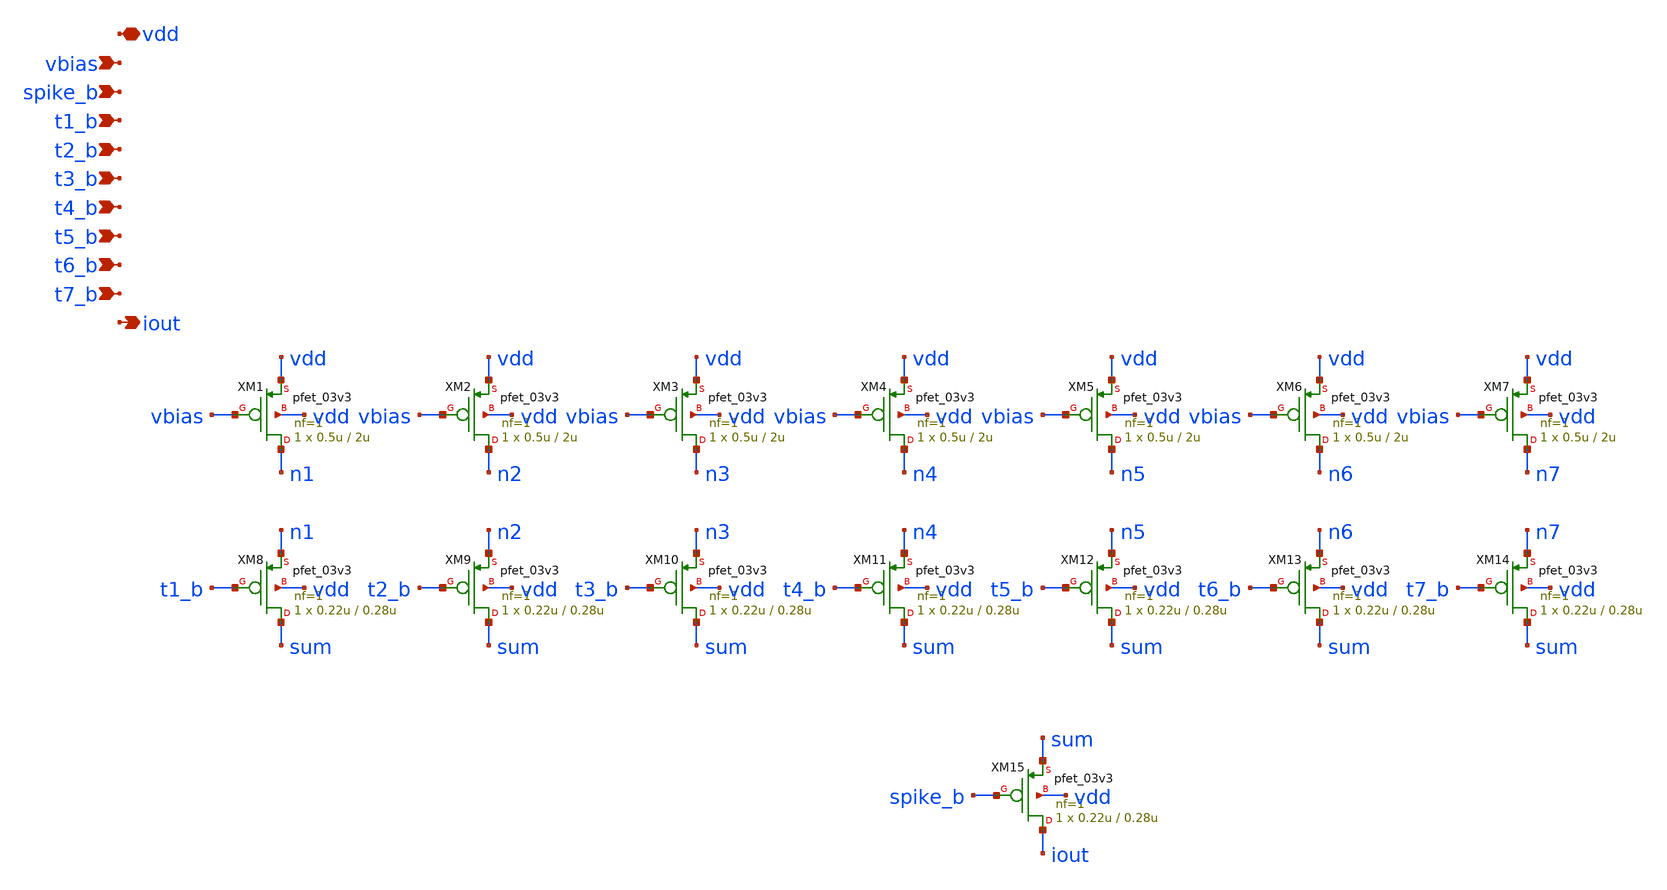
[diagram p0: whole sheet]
** sch_path: analog/dac/unary_DAC.sch
**.subckt unary_DAC vdd vbias spike_b t1_b t2_b t3_b t4_b t5_b t6_b t7_b iout
*.iopin vdd
*.ipin vbias
*.ipin spike_b
*.ipin t1_b
*.ipin t2_b
*.ipin t3_b
*.ipin t4_b
*.ipin t5_b
*.ipin t6_b
*.ipin t7_b
*.opin iout
XM1 n1 vbias vdd vdd pfet_03v3 L=2u W=0.5u nf=1 ad='int((nf+1)/2) * W/nf * 0.18u' as='int((nf+2)/2) * W/nf * 0.18u'
+ pd='2*int((nf+1)/2) * (W/nf + 0.18u)' ps='2*int((nf+2)/2) * (W/nf + 0.18u)' nrd='0.18u / W' nrs='0.18u / W'
+ sa=0 sb=0 sd=0 m=1
XM8 sum t1_b n1 vdd pfet_03v3 L=0.28u W=0.22u nf=1 ad='int((nf+1)/2) * W/nf * 0.18u' as='int((nf+2)/2) * W/nf * 0.18u'
+ pd='2*int((nf+1)/2) * (W/nf + 0.18u)' ps='2*int((nf+2)/2) * (W/nf + 0.18u)' nrd='0.18u / W' nrs='0.18u / W'
+ sa=0 sb=0 sd=0 m=1
XM2 n2 vbias vdd vdd pfet_03v3 L=2u W=0.5u nf=1 ad='int((nf+1)/2) * W/nf * 0.18u' as='int((nf+2)/2) * W/nf * 0.18u'
+ pd='2*int((nf+1)/2) * (W/nf + 0.18u)' ps='2*int((nf+2)/2) * (W/nf + 0.18u)' nrd='0.18u / W' nrs='0.18u / W'
+ sa=0 sb=0 sd=0 m=1
XM9 sum t2_b n2 vdd pfet_03v3 L=0.28u W=0.22u nf=1 ad='int((nf+1)/2) * W/nf * 0.18u' as='int((nf+2)/2) * W/nf * 0.18u'
+ pd='2*int((nf+1)/2) * (W/nf + 0.18u)' ps='2*int((nf+2)/2) * (W/nf + 0.18u)' nrd='0.18u / W' nrs='0.18u / W'
+ sa=0 sb=0 sd=0 m=1
XM3 n3 vbias vdd vdd pfet_03v3 L=2u W=0.5u nf=1 ad='int((nf+1)/2) * W/nf * 0.18u' as='int((nf+2)/2) * W/nf * 0.18u'
+ pd='2*int((nf+1)/2) * (W/nf + 0.18u)' ps='2*int((nf+2)/2) * (W/nf + 0.18u)' nrd='0.18u / W' nrs='0.18u / W'
+ sa=0 sb=0 sd=0 m=1
XM10 sum t3_b n3 vdd pfet_03v3 L=0.28u W=0.22u nf=1 ad='int((nf+1)/2) * W/nf * 0.18u' as='int((nf+2)/2) * W/nf * 0.18u'
+ pd='2*int((nf+1)/2) * (W/nf + 0.18u)' ps='2*int((nf+2)/2) * (W/nf + 0.18u)' nrd='0.18u / W' nrs='0.18u / W'
+ sa=0 sb=0 sd=0 m=1
XM4 n4 vbias vdd vdd pfet_03v3 L=2u W=0.5u nf=1 ad='int((nf+1)/2) * W/nf * 0.18u' as='int((nf+2)/2) * W/nf * 0.18u'
+ pd='2*int((nf+1)/2) * (W/nf + 0.18u)' ps='2*int((nf+2)/2) * (W/nf + 0.18u)' nrd='0.18u / W' nrs='0.18u / W'
+ sa=0 sb=0 sd=0 m=1
XM11 sum t4_b n4 vdd pfet_03v3 L=0.28u W=0.22u nf=1 ad='int((nf+1)/2) * W/nf * 0.18u' as='int((nf+2)/2) * W/nf * 0.18u'
+ pd='2*int((nf+1)/2) * (W/nf + 0.18u)' ps='2*int((nf+2)/2) * (W/nf + 0.18u)' nrd='0.18u / W' nrs='0.18u / W'
+ sa=0 sb=0 sd=0 m=1
XM5 n5 vbias vdd vdd pfet_03v3 L=2u W=0.5u nf=1 ad='int((nf+1)/2) * W/nf * 0.18u' as='int((nf+2)/2) * W/nf * 0.18u'
+ pd='2*int((nf+1)/2) * (W/nf + 0.18u)' ps='2*int((nf+2)/2) * (W/nf + 0.18u)' nrd='0.18u / W' nrs='0.18u / W'
+ sa=0 sb=0 sd=0 m=1
XM12 sum t5_b n5 vdd pfet_03v3 L=0.28u W=0.22u nf=1 ad='int((nf+1)/2) * W/nf * 0.18u' as='int((nf+2)/2) * W/nf * 0.18u'
+ pd='2*int((nf+1)/2) * (W/nf + 0.18u)' ps='2*int((nf+2)/2) * (W/nf + 0.18u)' nrd='0.18u / W' nrs='0.18u / W'
+ sa=0 sb=0 sd=0 m=1
XM6 n6 vbias vdd vdd pfet_03v3 L=2u W=0.5u nf=1 ad='int((nf+1)/2) * W/nf * 0.18u' as='int((nf+2)/2) * W/nf * 0.18u'
+ pd='2*int((nf+1)/2) * (W/nf + 0.18u)' ps='2*int((nf+2)/2) * (W/nf + 0.18u)' nrd='0.18u / W' nrs='0.18u / W'
+ sa=0 sb=0 sd=0 m=1
XM13 sum t6_b n6 vdd pfet_03v3 L=0.28u W=0.22u nf=1 ad='int((nf+1)/2) * W/nf * 0.18u' as='int((nf+2)/2) * W/nf * 0.18u'
+ pd='2*int((nf+1)/2) * (W/nf + 0.18u)' ps='2*int((nf+2)/2) * (W/nf + 0.18u)' nrd='0.18u / W' nrs='0.18u / W'
+ sa=0 sb=0 sd=0 m=1
XM7 n7 vbias vdd vdd pfet_03v3 L=2u W=0.5u nf=1 ad='int((nf+1)/2) * W/nf * 0.18u' as='int((nf+2)/2) * W/nf * 0.18u'
+ pd='2*int((nf+1)/2) * (W/nf + 0.18u)' ps='2*int((nf+2)/2) * (W/nf + 0.18u)' nrd='0.18u / W' nrs='0.18u / W'
+ sa=0 sb=0 sd=0 m=1
XM14 sum t7_b n7 vdd pfet_03v3 L=0.28u W=0.22u nf=1 ad='int((nf+1)/2) * W/nf * 0.18u' as='int((nf+2)/2) * W/nf * 0.18u'
+ pd='2*int((nf+1)/2) * (W/nf + 0.18u)' ps='2*int((nf+2)/2) * (W/nf + 0.18u)' nrd='0.18u / W' nrs='0.18u / W'
+ sa=0 sb=0 sd=0 m=1
XM15 iout spike_b sum vdd pfet_03v3 L=0.28u W=0.22u nf=1 ad='int((nf+1)/2) * W/nf * 0.18u' as='int((nf+2)/2) * W/nf * 0.18u'
+ pd='2*int((nf+1)/2) * (W/nf + 0.18u)' ps='2*int((nf+2)/2) * (W/nf + 0.18u)' nrd='0.18u / W' nrs='0.18u / W'
+ sa=0 sb=0 sd=0 m=1
**.ends
.end
